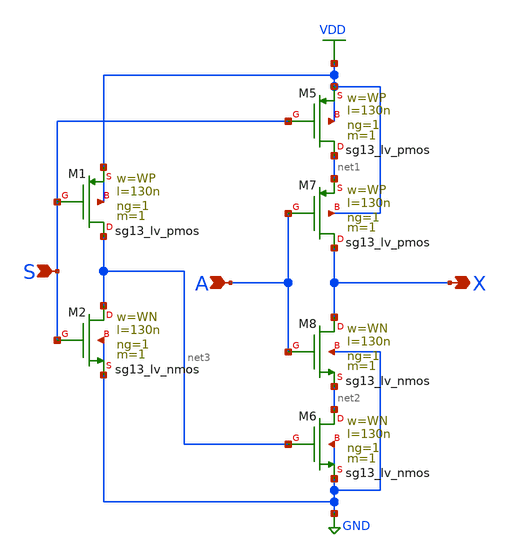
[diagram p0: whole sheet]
** sch_path: Tile/include/cmos5l/konrads_cells/sch/tri_buff_cell.sch
**.subckt tri_buff_cell A S X
*.ipin A
*.ipin S
*.opin X
XM5 net1 S VDD VDD sg13_lv_pmos w=WP l=130n ng=1 m=1 mm_ok=1
XM6 net2 net3 GND GND sg13_lv_nmos w=WN l=130n ng=1 m=1 mm_ok=1
XM7 X A net1 VDD sg13_lv_pmos w=WP l=130n ng=1 m=1 mm_ok=1
XM8 X A net2 GND sg13_lv_nmos w=WN l=130n ng=1 m=1 mm_ok=1
XM1 net3 S VDD VDD sg13_lv_pmos w=WP l=130n ng=1 m=1 mm_ok=1
XM2 net3 S GND GND sg13_lv_nmos w=WN l=130n ng=1 m=1 mm_ok=1
**.ends
.GLOBAL VDD
.GLOBAL GND
.end
